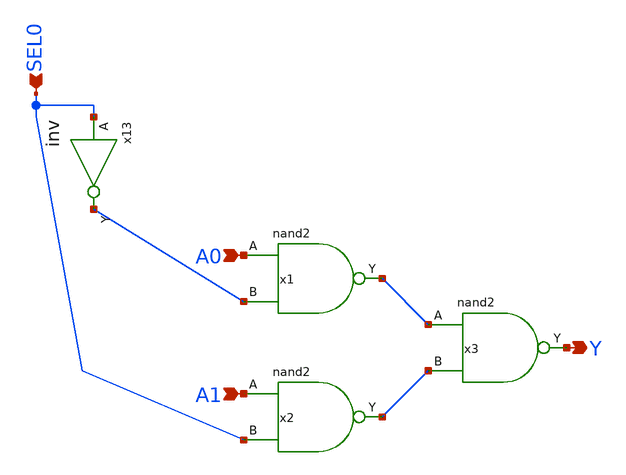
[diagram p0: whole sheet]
** sch_path: design/xschem/MUX/mux2efe.sch
**.subckt mux2efe SEL0 A0 A1 Y
*.ipin SEL0
*.ipin A0
*.ipin A1
*.opin Y
x1 A0 net3 VSS VDD net1 nand2
x2 A1 SEL0 VSS VDD net2 nand2
x13 SEL0 VSS VDD net3 inv
x3 net1 net2 VSS VDD Y nand2
**.ends

* expanding   symbol:  NAND/nand2.sym # of pins=3
** sym_path: design/xschem/NAND/nand2.sym
** sch_path: design/xschem/NAND/nand2.sch
.subckt nand2 A B VSS VDD Y
*.ipin A
*.opin Y
*.ipin B
XM1 Y A VDD VDD sky130_fd_pr__pfet_01v8 L=0.15 W=3.2 nf=1 ad='int((nf+1)/2) * W/nf * 0.29' as='int((nf+2)/2) * W/nf * 0.29'
+ pd='2*int((nf+1)/2) * (W/nf + 0.29)' ps='2*int((nf+2)/2) * (W/nf + 0.29)' nrd='0.29 / W' nrs='0.29 / W'
+ sa=0 sb=0 sd=0 mult=1 m=1
XM2 Y A net1 net1 sky130_fd_pr__nfet_01v8 L=0.15 W=2 nf=1 ad='int((nf+1)/2) * W/nf * 0.29' as='int((nf+2)/2) * W/nf * 0.29'
+ pd='2*int((nf+1)/2) * (W/nf + 0.29)' ps='2*int((nf+2)/2) * (W/nf + 0.29)' nrd='0.29 / W' nrs='0.29 / W'
+ sa=0 sb=0 sd=0 mult=1 m=1
XM3 net1 B VSS VSS sky130_fd_pr__nfet_01v8 L=0.15 W=2 nf=1 ad='int((nf+1)/2) * W/nf * 0.29' as='int((nf+2)/2) * W/nf * 0.29'
+ pd='2*int((nf+1)/2) * (W/nf + 0.29)' ps='2*int((nf+2)/2) * (W/nf + 0.29)' nrd='0.29 / W' nrs='0.29 / W'
+ sa=0 sb=0 sd=0 mult=1 m=1
XM4 Y B VDD VDD sky130_fd_pr__pfet_01v8 L=0.15 W=3.2 nf=1 ad='int((nf+1)/2) * W/nf * 0.29' as='int((nf+2)/2) * W/nf * 0.29'
+ pd='2*int((nf+1)/2) * (W/nf + 0.29)' ps='2*int((nf+2)/2) * (W/nf + 0.29)' nrd='0.29 / W' nrs='0.29 / W'
+ sa=0 sb=0 sd=0 mult=1 m=1
.ends


* expanding   symbol:  INV/inv.sym # of pins=2
** sym_path: design/xschem/INV/inv.sym
** sch_path: design/xschem/INV/inv.sch
.subckt inv A VSS VDD Y
*.ipin A
*.opin Y
XM2 Y A VSS GND sky130_fd_pr__nfet_01v8 L=0.15 W=1 nf=1 ad='int((nf+1)/2) * W/nf * 0.29' as='int((nf+2)/2) * W/nf * 0.29'
+ pd='2*int((nf+1)/2) * (W/nf + 0.29)' ps='2*int((nf+2)/2) * (W/nf + 0.29)' nrd='0.29 / W' nrs='0.29 / W'
+ sa=0 sb=0 sd=0 mult=1 m=1
XM1 Y A VDD VDD sky130_fd_pr__pfet_01v8 L=0.15 W=3.21 nf=1 ad='int((nf+1)/2) * W/nf * 0.29' as='int((nf+2)/2) * W/nf * 0.29'
+ pd='2*int((nf+1)/2) * (W/nf + 0.29)' ps='2*int((nf+2)/2) * (W/nf + 0.29)' nrd='0.29 / W' nrs='0.29 / W'
+ sa=0 sb=0 sd=0 mult=1 m=1
.ends

.end
